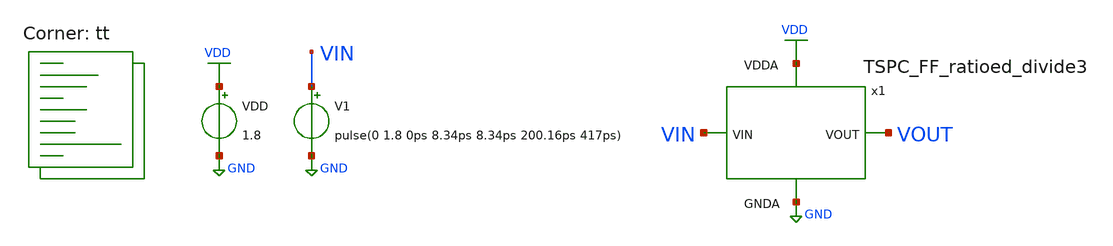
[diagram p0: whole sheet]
** sch_path: projects/pll/divider/xschem_ngspice/tb_TSPC_FF_ratioed_divide3_6.sch
**.subckt tb_TSPC_FF_ratioed_divide3_6
VDD VDD GND 1.8
V1 VIN GND pulse(0 1.8 0ps 8.34ps 8.34ps 200.16ps 417ps)
x1 VOUT VIN VDD GND TSPC_FF_ratioed_divide3
**** begin user architecture code



.include /foss/pdks/sky130A/libs.ref/sky130_fd_sc_hd/spice/sky130_fd_sc_hd.spice

.option method=gear
.option wnflag=1
* .option savecurrents


*.ic v(d)=0
*.ic v(q)=0
*.ic v(q1)=0

.probe p(x1)

.control

  save v(vin) v(vout) p(x1:power)
  * save all
  * tran 0.1n 1u
  tran 2p 10n

  remzerovec
  write tb_TSPC_FF_ratioed_divide3_6.raw
  * set appendwrite

.endc



.lib $::SKYWATER_MODELS/sky130.lib.spice tt
**** end user architecture code
**.ends

* expanding   symbol:
*+  /foss/designs/my_design/projects/pll/divider/xschem_ngspice/TSPC_FF_ratioed_divide3.sym # of pins=4
** sym_path: projects/pll/divider/xschem_ngspice/TSPC_FF_ratioed_divide3.sym
** sch_path: projects/pll/divider/xschem_ngspice/TSPC_FF_ratioed_divide3.sch
.subckt TSPC_FF_ratioed_divide3 VOUT VIN VDDA GNDA
*.ipin VIN
*.opin VOUT
*.ipin VDDA
*.ipin GNDA
XM24 net7 VIN VDDA VDDA sky130_fd_pr__pfet_01v8 L=0.15 W=0.43 nf=1 ad='int((nf+1)/2) * W/nf * 0.29' as='int((nf+2)/2) * W/nf * 0.29'
+ pd='2*int((nf+1)/2) * (W/nf + 0.29)' ps='2*int((nf+2)/2) * (W/nf + 0.29)' nrd='0.29 / W' nrs='0.29 / W'
+ sa=0 sb=0 sd=0 mult=1 m=1
XM29 net7 net1 GNDA GNDA sky130_fd_pr__nfet_01v8 L=0.15 W=0.43 nf=1 ad='int((nf+1)/2) * W/nf * 0.29'
+ as='int((nf+2)/2) * W/nf * 0.29' pd='2*int((nf+1)/2) * (W/nf + 0.29)' ps='2*int((nf+2)/2) * (W/nf + 0.29)'
+ nrd='0.29 / W' nrs='0.29 / W' sa=0 sb=0 sd=0 mult=1 m=1
XM30 net1 net2 VDDA VDDA sky130_fd_pr__pfet_01v8 L=0.15 W=0.43 nf=1 ad='int((nf+1)/2) * W/nf * 0.29'
+ as='int((nf+2)/2) * W/nf * 0.29' pd='2*int((nf+1)/2) * (W/nf + 0.29)' ps='2*int((nf+2)/2) * (W/nf + 0.29)'
+ nrd='0.29 / W' nrs='0.29 / W' sa=0 sb=0 sd=0 mult=1 m=1
XM31 net1 VIN GNDA GNDA sky130_fd_pr__nfet_01v8 L=0.15 W=1.5 nf=1 ad='int((nf+1)/2) * W/nf * 0.29' as='int((nf+2)/2) * W/nf * 0.29'
+ pd='2*int((nf+1)/2) * (W/nf + 0.29)' ps='2*int((nf+2)/2) * (W/nf + 0.29)' nrd='0.29 / W' nrs='0.29 / W'
+ sa=0 sb=0 sd=0 mult=1 m=1
XM32 net2 VOUT VDDA VDDA sky130_fd_pr__pfet_01v8 L=0.15 W=0.43 nf=1 ad='int((nf+1)/2) * W/nf * 0.29'
+ as='int((nf+2)/2) * W/nf * 0.29' pd='2*int((nf+1)/2) * (W/nf + 0.29)' ps='2*int((nf+2)/2) * (W/nf + 0.29)'
+ nrd='0.29 / W' nrs='0.29 / W' sa=0 sb=0 sd=0 mult=1 m=1
XM33 net8 VOUT GNDA GNDA sky130_fd_pr__nfet_01v8 L=0.15 W=0.43 nf=1 ad='int((nf+1)/2) * W/nf * 0.29'
+ as='int((nf+2)/2) * W/nf * 0.29' pd='2*int((nf+1)/2) * (W/nf + 0.29)' ps='2*int((nf+2)/2) * (W/nf + 0.29)'
+ nrd='0.29 / W' nrs='0.29 / W' sa=0 sb=0 sd=0 mult=1 m=1
XM28 net2 VIN net8 GNDA sky130_fd_pr__nfet_01v8 L=0.15 W=0.43 nf=1 ad='int((nf+1)/2) * W/nf * 0.29' as='int((nf+2)/2) * W/nf * 0.29'
+ pd='2*int((nf+1)/2) * (W/nf + 0.29)' ps='2*int((nf+2)/2) * (W/nf + 0.29)' nrd='0.29 / W' nrs='0.29 / W'
+ sa=0 sb=0 sd=0 mult=1 m=1
XM34 net6 VIN VDDA VDDA sky130_fd_pr__pfet_01v8 L=0.15 W=0.43 nf=1 ad='int((nf+1)/2) * W/nf * 0.29' as='int((nf+2)/2) * W/nf * 0.29'
+ pd='2*int((nf+1)/2) * (W/nf + 0.29)' ps='2*int((nf+2)/2) * (W/nf + 0.29)' nrd='0.29 / W' nrs='0.29 / W'
+ sa=0 sb=0 sd=0 mult=1 m=1
XM39 net6 net4 GNDA GNDA sky130_fd_pr__nfet_01v8 L=0.15 W=0.43 nf=1 ad='int((nf+1)/2) * W/nf * 0.29'
+ as='int((nf+2)/2) * W/nf * 0.29' pd='2*int((nf+1)/2) * (W/nf + 0.29)' ps='2*int((nf+2)/2) * (W/nf + 0.29)'
+ nrd='0.29 / W' nrs='0.29 / W' sa=0 sb=0 sd=0 mult=1 m=1
XM40 net4 net5 VDDA VDDA sky130_fd_pr__pfet_01v8 L=0.15 W=0.43 nf=1 ad='int((nf+1)/2) * W/nf * 0.29'
+ as='int((nf+2)/2) * W/nf * 0.29' pd='2*int((nf+1)/2) * (W/nf + 0.29)' ps='2*int((nf+2)/2) * (W/nf + 0.29)'
+ nrd='0.29 / W' nrs='0.29 / W' sa=0 sb=0 sd=0 mult=1 m=1
XM41 net4 VIN GNDA GNDA sky130_fd_pr__nfet_01v8 L=0.15 W=1.5 nf=1 ad='int((nf+1)/2) * W/nf * 0.29' as='int((nf+2)/2) * W/nf * 0.29'
+ pd='2*int((nf+1)/2) * (W/nf + 0.29)' ps='2*int((nf+2)/2) * (W/nf + 0.29)' nrd='0.29 / W' nrs='0.29 / W'
+ sa=0 sb=0 sd=0 mult=1 m=1
XM42 net5 net6 VDDA VDDA sky130_fd_pr__pfet_01v8 L=0.15 W=0.43 nf=1 ad='int((nf+1)/2) * W/nf * 0.29'
+ as='int((nf+2)/2) * W/nf * 0.29' pd='2*int((nf+1)/2) * (W/nf + 0.29)' ps='2*int((nf+2)/2) * (W/nf + 0.29)'
+ nrd='0.29 / W' nrs='0.29 / W' sa=0 sb=0 sd=0 mult=1 m=1
XM43 net9 net7 net3 GNDA sky130_fd_pr__nfet_01v8 L=0.15 W=0.43 nf=1 ad='int((nf+1)/2) * W/nf * 0.29'
+ as='int((nf+2)/2) * W/nf * 0.29' pd='2*int((nf+1)/2) * (W/nf + 0.29)' ps='2*int((nf+2)/2) * (W/nf + 0.29)'
+ nrd='0.29 / W' nrs='0.29 / W' sa=0 sb=0 sd=0 mult=1 m=1
XM44 net5 VIN net9 GNDA sky130_fd_pr__nfet_01v8 L=0.15 W=0.43 nf=1 ad='int((nf+1)/2) * W/nf * 0.29' as='int((nf+2)/2) * W/nf * 0.29'
+ pd='2*int((nf+1)/2) * (W/nf + 0.29)' ps='2*int((nf+2)/2) * (W/nf + 0.29)' nrd='0.29 / W' nrs='0.29 / W'
+ sa=0 sb=0 sd=0 mult=1 m=1
XM4 VOUT net6 VDDA VDDA sky130_fd_pr__pfet_01v8 L=0.15 W=0.86 nf=2 ad='int((nf+1)/2) * W/nf * 0.29' as='int((nf+2)/2) * W/nf * 0.29'
+ pd='2*int((nf+1)/2) * (W/nf + 0.29)' ps='2*int((nf+2)/2) * (W/nf + 0.29)' nrd='0.29 / W' nrs='0.29 / W'
+ sa=0 sb=0 sd=0 mult=1 m=1
XM5 VOUT net6 GNDA GNDA sky130_fd_pr__nfet_01v8 L=0.15 W=0.43 nf=1 ad='int((nf+1)/2) * W/nf * 0.29' as='int((nf+2)/2) * W/nf * 0.29'
+ pd='2*int((nf+1)/2) * (W/nf + 0.29)' ps='2*int((nf+2)/2) * (W/nf + 0.29)' nrd='0.29 / W' nrs='0.29 / W'
+ sa=0 sb=0 sd=0 mult=1 m=1
XM6 net3 net6 GNDA GNDA sky130_fd_pr__nfet_01v8 L=0.15 W=0.43 nf=1 ad='int((nf+1)/2) * W/nf * 0.29' as='int((nf+2)/2) * W/nf * 0.29'
+ pd='2*int((nf+1)/2) * (W/nf + 0.29)' ps='2*int((nf+2)/2) * (W/nf + 0.29)' nrd='0.29 / W' nrs='0.29 / W'
+ sa=0 sb=0 sd=0 mult=1 m=1
XM7 net5 net7 VDDA VDDA sky130_fd_pr__pfet_01v8 L=0.15 W=0.43 nf=1 ad='int((nf+1)/2) * W/nf * 0.29' as='int((nf+2)/2) * W/nf * 0.29'
+ pd='2*int((nf+1)/2) * (W/nf + 0.29)' ps='2*int((nf+2)/2) * (W/nf + 0.29)' nrd='0.29 / W' nrs='0.29 / W'
+ sa=0 sb=0 sd=0 mult=1 m=1
.ends

.GLOBAL GND
.GLOBAL VDD
.end
